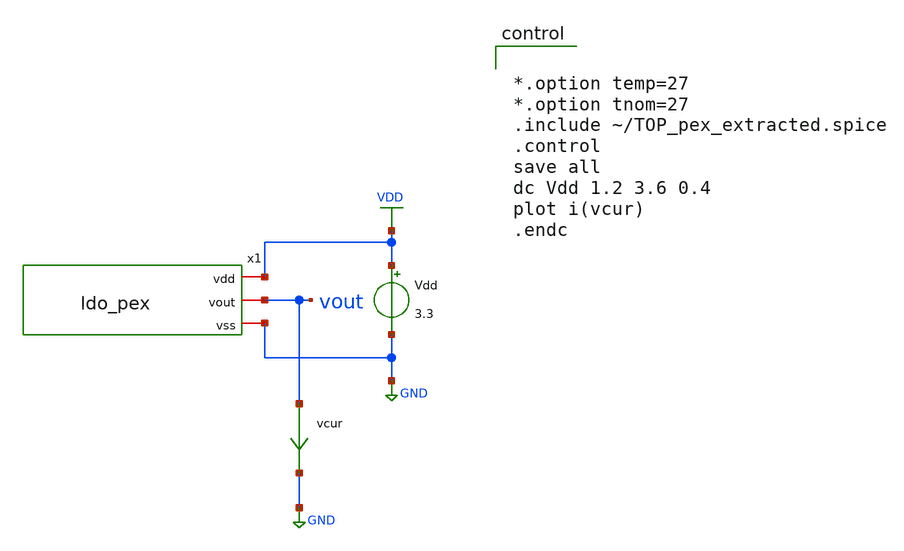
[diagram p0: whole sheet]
** sch_path: noritsuna/ldo/1st_version/ldo_pex_tb.sch
**.subckt ldo_pex_tb
Vdd VDD GND 3.3
vcur vout GND 0
.save i(vcur)
x1 vout VDD GND TOP
**** begin user architecture code


*.option temp=27
*.option tnom=27
.include ~/TOP_pex_extracted.spice
.control
save all
dc Vdd 1.2 3.6 0.4
plot i(vcur)
.endc


.include $::180MCU_MODELS/design.ngspice
.lib $::180MCU_MODELS/sm141064.ngspice typical
.lib $::180MCU_MODELS/sm141064.ngspice res_typical
.lib $::180MCU_MODELS/sm141064.ngspice cap_mim
.lib $::180MCU_MODELS/sm141064.ngspice moscap_typical
.lib $::180MCU_MODELS/sm141064.ngspice mimcap_typical
.lib $::180MCU_MODELS/sm141064.ngspice bjt_typical
* .lib $::180MCU_MODELS/sm141064.ngspice res_statistical
.include $::180MCU_STDCELLS/gf180mcu_fd_sc_mcu7t5v0.spice

**** end user architecture code
**.ends
.GLOBAL VDD
.GLOBAL GND
.end
